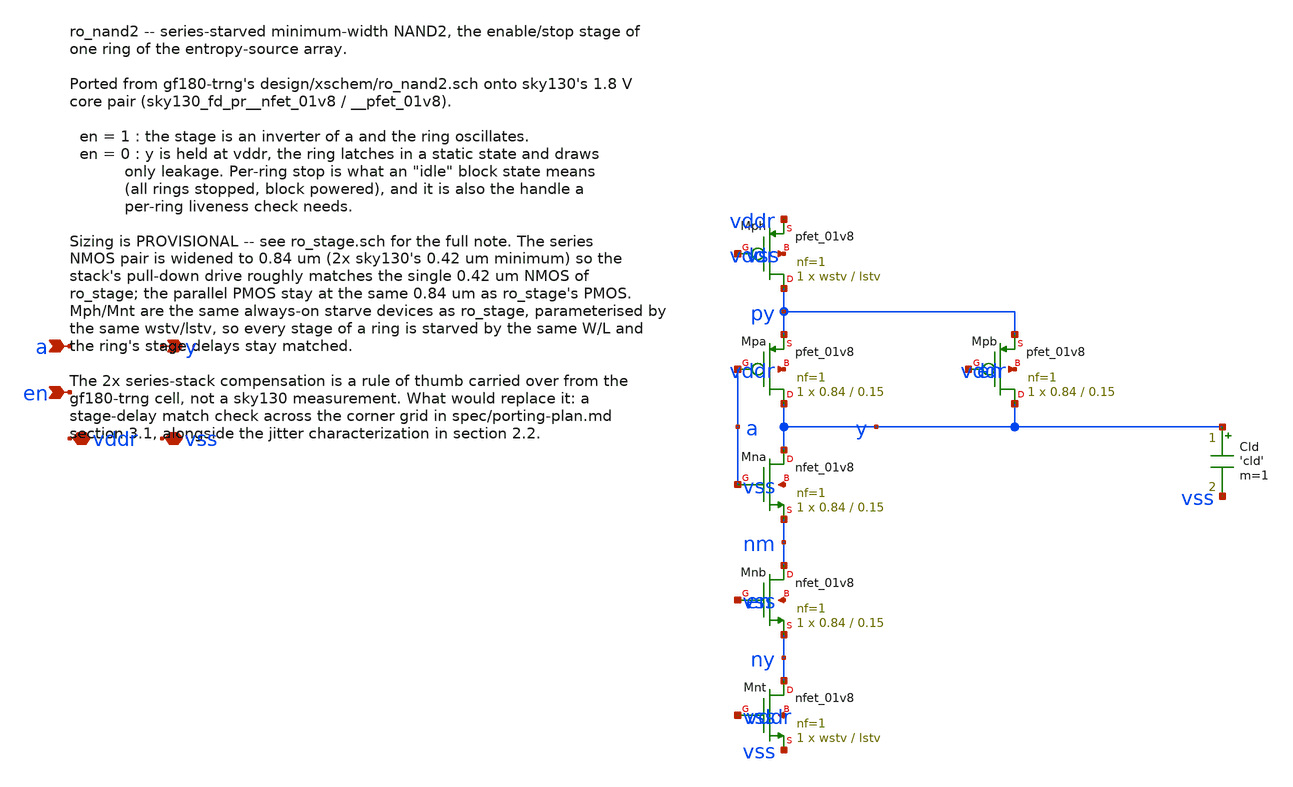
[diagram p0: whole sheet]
** sch_path: design/xschem/ro_nand2.sch
**.subckt ro_nand2 a en y vddr vss
*.ipin a
*.ipin en
*.opin y
*.iopin vddr
*.iopin vss
XMph py vss vddr vddr sky130_fd_pr__pfet_01v8 L=lstv W=wstv nf=1 ad='int((nf+1)/2) * W/nf * 0.29' as='int((nf+2)/2) * W/nf * 0.29'
+ pd='2*int((nf+1)/2) * (W/nf + 0.29)' ps='2*int((nf+2)/2) * (W/nf + 0.29)' nrd='0.29 / W' nrs='0.29 / W'
+ sa=0 sb=0 sd=0 mult=1 m=1
XMpa y a py vddr sky130_fd_pr__pfet_01v8 L=0.15 W=0.84 nf=1 ad='int((nf+1)/2) * W/nf * 0.29' as='int((nf+2)/2) * W/nf * 0.29'
+ pd='2*int((nf+1)/2) * (W/nf + 0.29)' ps='2*int((nf+2)/2) * (W/nf + 0.29)' nrd='0.29 / W' nrs='0.29 / W'
+ sa=0 sb=0 sd=0 mult=1 m=1
XMpb y en py vddr sky130_fd_pr__pfet_01v8 L=0.15 W=0.84 nf=1 ad='int((nf+1)/2) * W/nf * 0.29' as='int((nf+2)/2) * W/nf * 0.29'
+ pd='2*int((nf+1)/2) * (W/nf + 0.29)' ps='2*int((nf+2)/2) * (W/nf + 0.29)' nrd='0.29 / W' nrs='0.29 / W'
+ sa=0 sb=0 sd=0 mult=1 m=1
XMna y a nm vss sky130_fd_pr__nfet_01v8 L=0.15 W=0.84 nf=1 ad='int((1 + 1)/2) * 0.84 / 1 * 0.29' as='int((1 + 2)/2) * 0.84 / 1 * 0.29'
+ pd='2*int((1 + 1)/2) * (0.84 / 1 + 0.29)' ps='2*int((1 + 2)/2) * (0.84 / 1 + 0.29)' nrd='0.29 / 0.84 '
+ nrs='0.29 / 0.84 ' sa=0 sb=0 sd=0 mult=1 m=1
XMnb nm en ny vss sky130_fd_pr__nfet_01v8 L=0.15 W=0.84 nf=1 ad='int((1 + 1)/2) * 0.84 / 1 * 0.29' as='int((1 + 2)/2) * 0.84 / 1 * 0.29'
+ pd='2*int((1 + 1)/2) * (0.84 / 1 + 0.29)' ps='2*int((1 + 2)/2) * (0.84 / 1 + 0.29)' nrd='0.29 / 0.84 '
+ nrs='0.29 / 0.84 ' sa=0 sb=0 sd=0 mult=1 m=1
XMnt ny vddr vss vss sky130_fd_pr__nfet_01v8 L=lstv W=wstv nf=1 ad='int((1 + 1)/2) * wstv / 1 * 0.29'
+ as='int((1 + 2)/2) * wstv / 1 * 0.29' pd='2*int((1 + 1)/2) * (wstv / 1 + 0.29)' ps='2*int((1 + 2)/2) * (wstv / 1 + 0.29)'
+ nrd='0.29 / wstv ' nrs='0.29 / wstv ' sa=0 sb=0 sd=0 mult=1 m=1
Cld y vss 'cld' m=1
**.ends
.end
